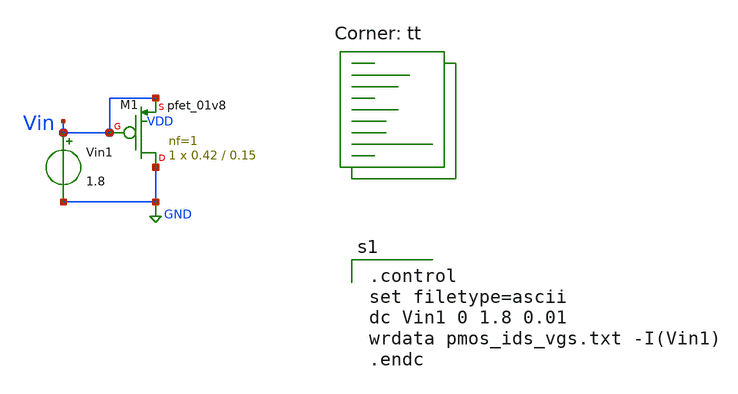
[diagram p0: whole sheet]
** sch_path: tut1/pmos/expt1_0/expt1_0.sch
**.subckt expt1_0
Vin1 Vin GND 1.8
XM1 GND Vin Vin VDD sky130_fd_pr__pfet_01v8 L=0.15 W=0.42 nf=1 ad='int((nf+1)/2) * W/nf * 0.29' as='int((nf+2)/2) * W/nf * 0.29'
+ pd='2*int((nf+1)/2) * (W/nf + 0.29)' ps='2*int((nf+2)/2) * (W/nf + 0.29)' nrd='0.29 / W' nrs='0.29 / W'
+ sa=0 sb=0 sd=0 mult=1 m=1
**** begin user architecture code
.lib $::SKYWATER_MODELS/sky130.lib.spice tt

.control
set filetype=ascii
dc Vin1 0 1.8 0.01
wrdata pmos_ids_vgs.txt -I(Vin1)
.endc

**** end user architecture code
**.ends
.GLOBAL GND
.end
